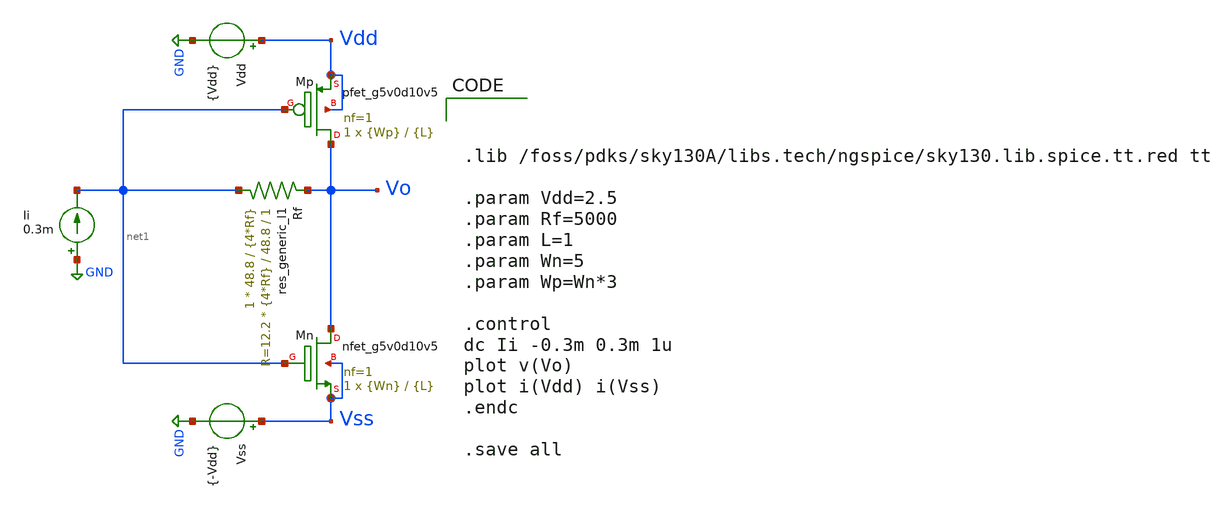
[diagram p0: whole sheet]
** sch_path: Vector-Matrix-Multiplicaction/xschem/TIA_design.sch
**.subckt TIA_design
XMp Vo net1 Vdd Vdd sky130_fd_pr__pfet_g5v0d10v5 L={L} W={Wp} nf=1 ad='int((nf+1)/2) * W/nf * 0.29' as='int((nf+2)/2) * W/nf * 0.29'
+ pd='2*int((nf+1)/2) * (W/nf + 0.29)' ps='2*int((nf+2)/2) * (W/nf + 0.29)' nrd='0.29 / W' nrs='0.29 / W'
+ sa=0 sb=0 sd=0 mult=1 m=1
XMn Vo net1 Vss Vss sky130_fd_pr__nfet_g5v0d10v5 L={L} W={Wn} nf=1 ad='int((nf+1)/2) * W/nf * 0.29' as='int((nf+2)/2) * W/nf * 0.29'
+ pd='2*int((nf+1)/2) * (W/nf + 0.29)' ps='2*int((nf+2)/2) * (W/nf + 0.29)' nrd='0.29 / W' nrs='0.29 / W'
+ sa=0 sb=0 sd=0 mult=1 m=1
Vdd Vdd GND {Vdd}
Vss Vss GND {-Vdd}
Ii GND net1 0.3m
Rf net1 Vo sky130_fd_pr__res_generic_l1 W=48.8 L={4*Rf} m=1
**** begin user architecture code



.lib /foss/pdks/sky130A/libs.tech/ngspice/sky130.lib.spice.tt.red tt

.param Vdd=2.5
.param Rf=5000
.param L=1
.param Wn=5
.param Wp=Wn*3

.control
dc Ii -0.3m 0.3m 1u
plot v(Vo)
plot i(Vdd) i(Vss)
.endc

.save all


**** end user architecture code
**.ends
.GLOBAL GND
.end
